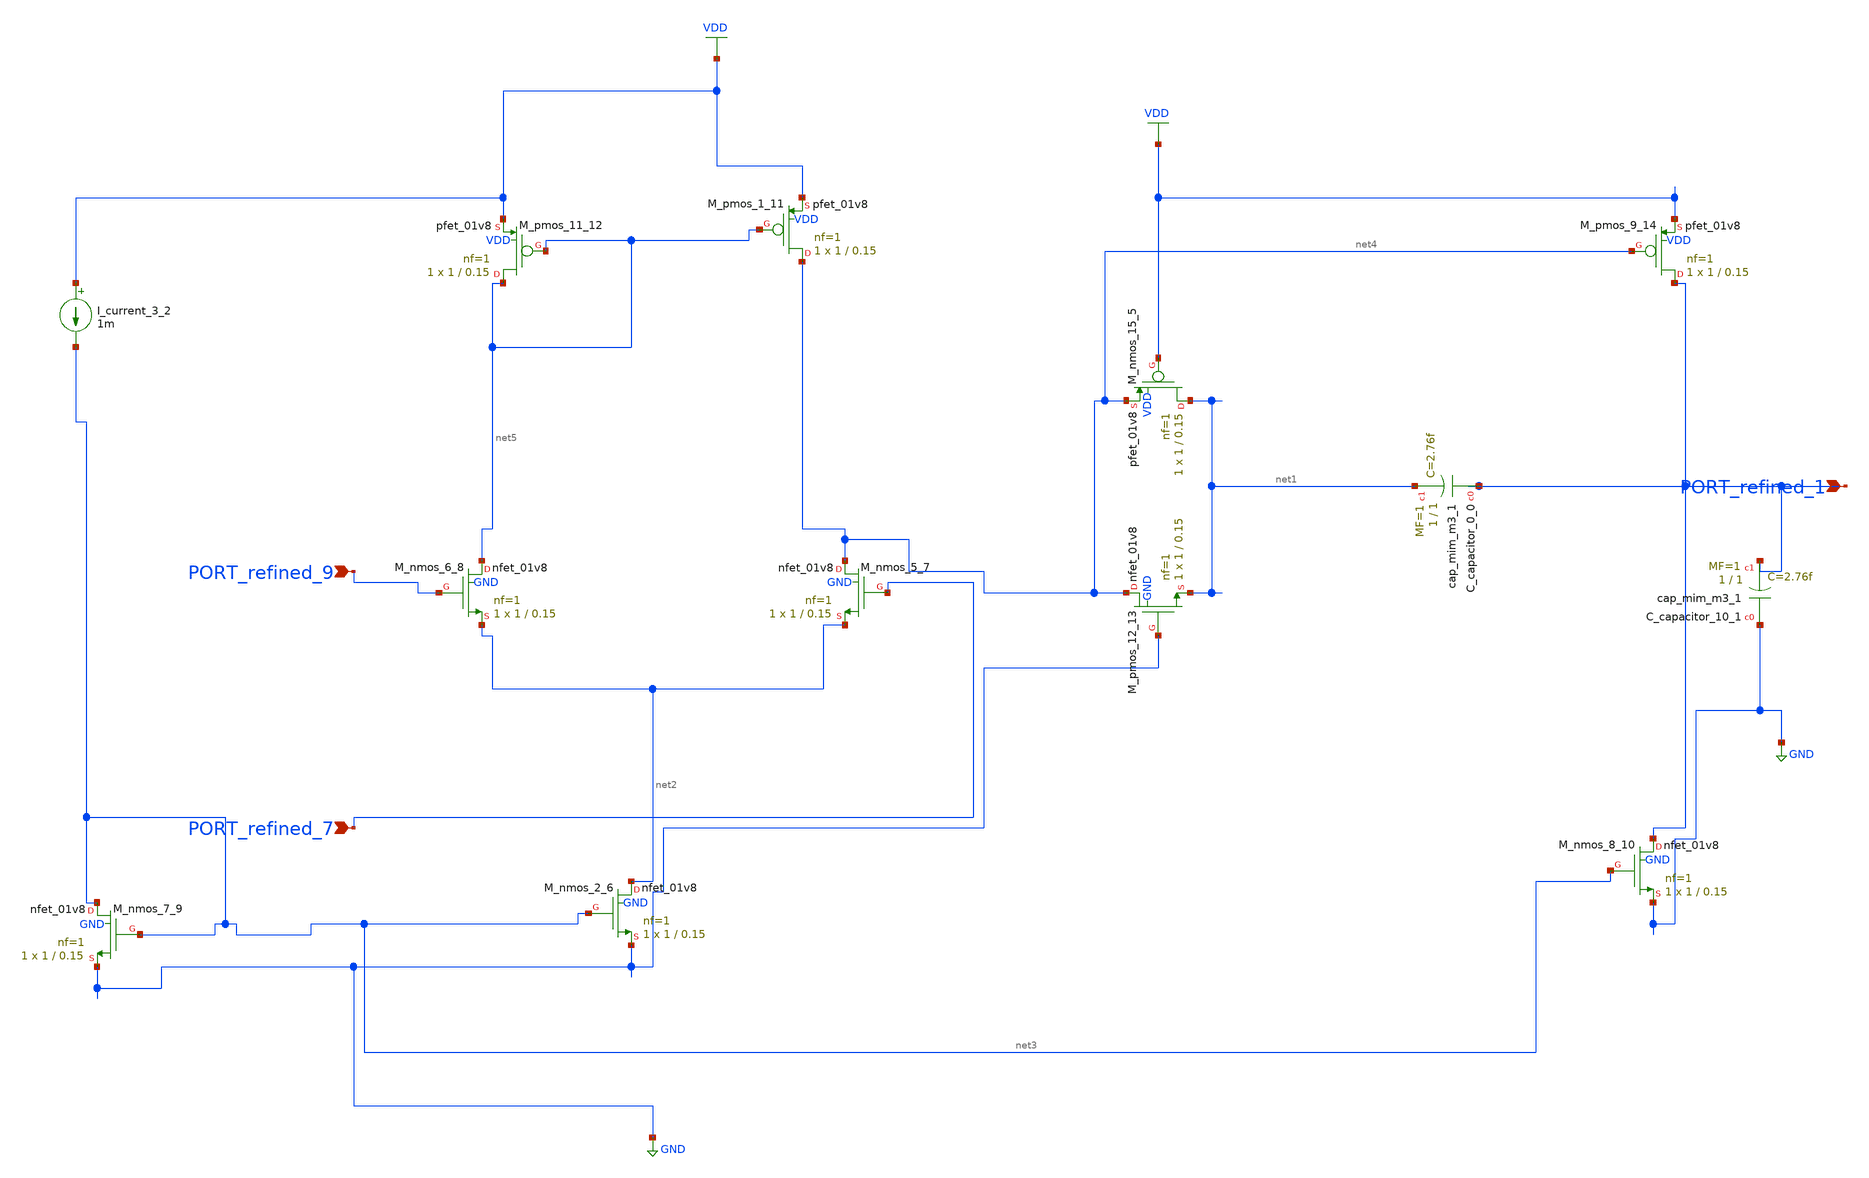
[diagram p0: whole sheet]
** sch_path: schematics/p02_fig2.sch
**.subckt p02_fig2 PORT_refined_9 PORT_refined_7 PORT_refined_1
*.ipin PORT_refined_9
*.ipin PORT_refined_7
*.ipin PORT_refined_1
XC_capacitor_0_0 PORT_refined_1 net1 sky130_fd_pr__cap_mim_m3_1 W=1 L=1 MF=1 m=1
XC_capacitor_10_1 GND PORT_refined_1 sky130_fd_pr__cap_mim_m3_1 W=1 L=1 MF=1 m=1
I_current_3_2 VDD net3 1m
XM_nmos_15_5 net1 VDD net4 VDD sky130_fd_pr__pfet_01v8 L=0.15 W=1 nf=1 ad='int((1 + 1)/2) * 1 / 1 * 0.29'
+ as='int((1 + 2)/2) * 1 / 1 * 0.29' pd='2*int((1 + 1)/2) * (1 / 1 + 0.29)' ps='2*int((1 + 2)/2) * (1 / 1 + 0.29)'
+ nrd='0.29 / 1 ' nrs='0.29 / 1 ' sa=0 sb=0 sd=0 mult=1 m=1
XM_nmos_2_6 net2 net3 GND GND sky130_fd_pr__nfet_01v8 L=0.15 W=1 nf=1 ad='int((1 + 1)/2) * 1 / 1 * 0.29'
+ as='int((1 + 2)/2) * 1 / 1 * 0.29' pd='2*int((1 + 1)/2) * (1 / 1 + 0.29)' ps='2*int((1 + 2)/2) * (1 / 1 + 0.29)'
+ nrd='0.29 / 1 ' nrs='0.29 / 1 ' sa=0 sb=0 sd=0 mult=1 m=1
XM_nmos_5_7 net4 PORT_refined_7 net2 GND sky130_fd_pr__nfet_01v8 L=0.15 W=1 nf=1 ad='int((1 + 1)/2) * 1 / 1 * 0.29'
+ as='int((1 + 2)/2) * 1 / 1 * 0.29' pd='2*int((1 + 1)/2) * (1 / 1 + 0.29)' ps='2*int((1 + 2)/2) * (1 / 1 + 0.29)'
+ nrd='0.29 / 1 ' nrs='0.29 / 1 ' sa=0 sb=0 sd=0 mult=1 m=1
XM_nmos_6_8 net5 PORT_refined_9 net2 GND sky130_fd_pr__nfet_01v8 L=0.15 W=1 nf=1 ad='int((1 + 1)/2) * 1 / 1 * 0.29'
+ as='int((1 + 2)/2) * 1 / 1 * 0.29' pd='2*int((1 + 1)/2) * (1 / 1 + 0.29)' ps='2*int((1 + 2)/2) * (1 / 1 + 0.29)'
+ nrd='0.29 / 1 ' nrs='0.29 / 1 ' sa=0 sb=0 sd=0 mult=1 m=1
XM_nmos_7_9 net3 net3 GND GND sky130_fd_pr__nfet_01v8 L=0.15 W=1 nf=1 ad='int((1 + 1)/2) * 1 / 1 * 0.29'
+ as='int((1 + 2)/2) * 1 / 1 * 0.29' pd='2*int((1 + 1)/2) * (1 / 1 + 0.29)' ps='2*int((1 + 2)/2) * (1 / 1 + 0.29)'
+ nrd='0.29 / 1 ' nrs='0.29 / 1 ' sa=0 sb=0 sd=0 mult=1 m=1
XM_nmos_8_10 PORT_refined_1 net3 GND GND sky130_fd_pr__nfet_01v8 L=0.15 W=1 nf=1 ad='int((1 + 1)/2) * 1 / 1 * 0.29'
+ as='int((1 + 2)/2) * 1 / 1 * 0.29' pd='2*int((1 + 1)/2) * (1 / 1 + 0.29)' ps='2*int((1 + 2)/2) * (1 / 1 + 0.29)'
+ nrd='0.29 / 1 ' nrs='0.29 / 1 ' sa=0 sb=0 sd=0 mult=1 m=1
XM_pmos_1_11 net4 net5 VDD VDD sky130_fd_pr__pfet_01v8 L=0.15 W=1 nf=1 ad='int((1 + 1)/2) * 1 / 1 * 0.29'
+ as='int((1 + 2)/2) * 1 / 1 * 0.29' pd='2*int((1 + 1)/2) * (1 / 1 + 0.29)' ps='2*int((1 + 2)/2) * (1 / 1 + 0.29)'
+ nrd='0.29 / 1 ' nrs='0.29 / 1 ' sa=0 sb=0 sd=0 mult=1 m=1
XM_pmos_11_12 net5 net5 VDD VDD sky130_fd_pr__pfet_01v8 L=0.15 W=1 nf=1 ad='int((1 + 1)/2) * 1 / 1 * 0.29'
+ as='int((1 + 2)/2) * 1 / 1 * 0.29' pd='2*int((1 + 1)/2) * (1 / 1 + 0.29)' ps='2*int((1 + 2)/2) * (1 / 1 + 0.29)'
+ nrd='0.29 / 1 ' nrs='0.29 / 1 ' sa=0 sb=0 sd=0 mult=1 m=1
XM_pmos_12_13 net4 GND net1 GND sky130_fd_pr__nfet_01v8 L=0.15 W=1 nf=1 ad='int((1 + 1)/2) * 1 / 1 * 0.29'
+ as='int((1 + 2)/2) * 1 / 1 * 0.29' pd='2*int((1 + 1)/2) * (1 / 1 + 0.29)' ps='2*int((1 + 2)/2) * (1 / 1 + 0.29)'
+ nrd='0.29 / 1 ' nrs='0.29 / 1 ' sa=0 sb=0 sd=0 mult=1 m=1
XM_pmos_9_14 PORT_refined_1 net4 VDD VDD sky130_fd_pr__pfet_01v8 L=0.15 W=1 nf=1 ad='int((1 + 1)/2) * 1 / 1 * 0.29'
+ as='int((1 + 2)/2) * 1 / 1 * 0.29' pd='2*int((1 + 1)/2) * (1 / 1 + 0.29)' ps='2*int((1 + 2)/2) * (1 / 1 + 0.29)'
+ nrd='0.29 / 1 ' nrs='0.29 / 1 ' sa=0 sb=0 sd=0 mult=1 m=1
**.ends
.GLOBAL GND
.GLOBAL VDD
.end
